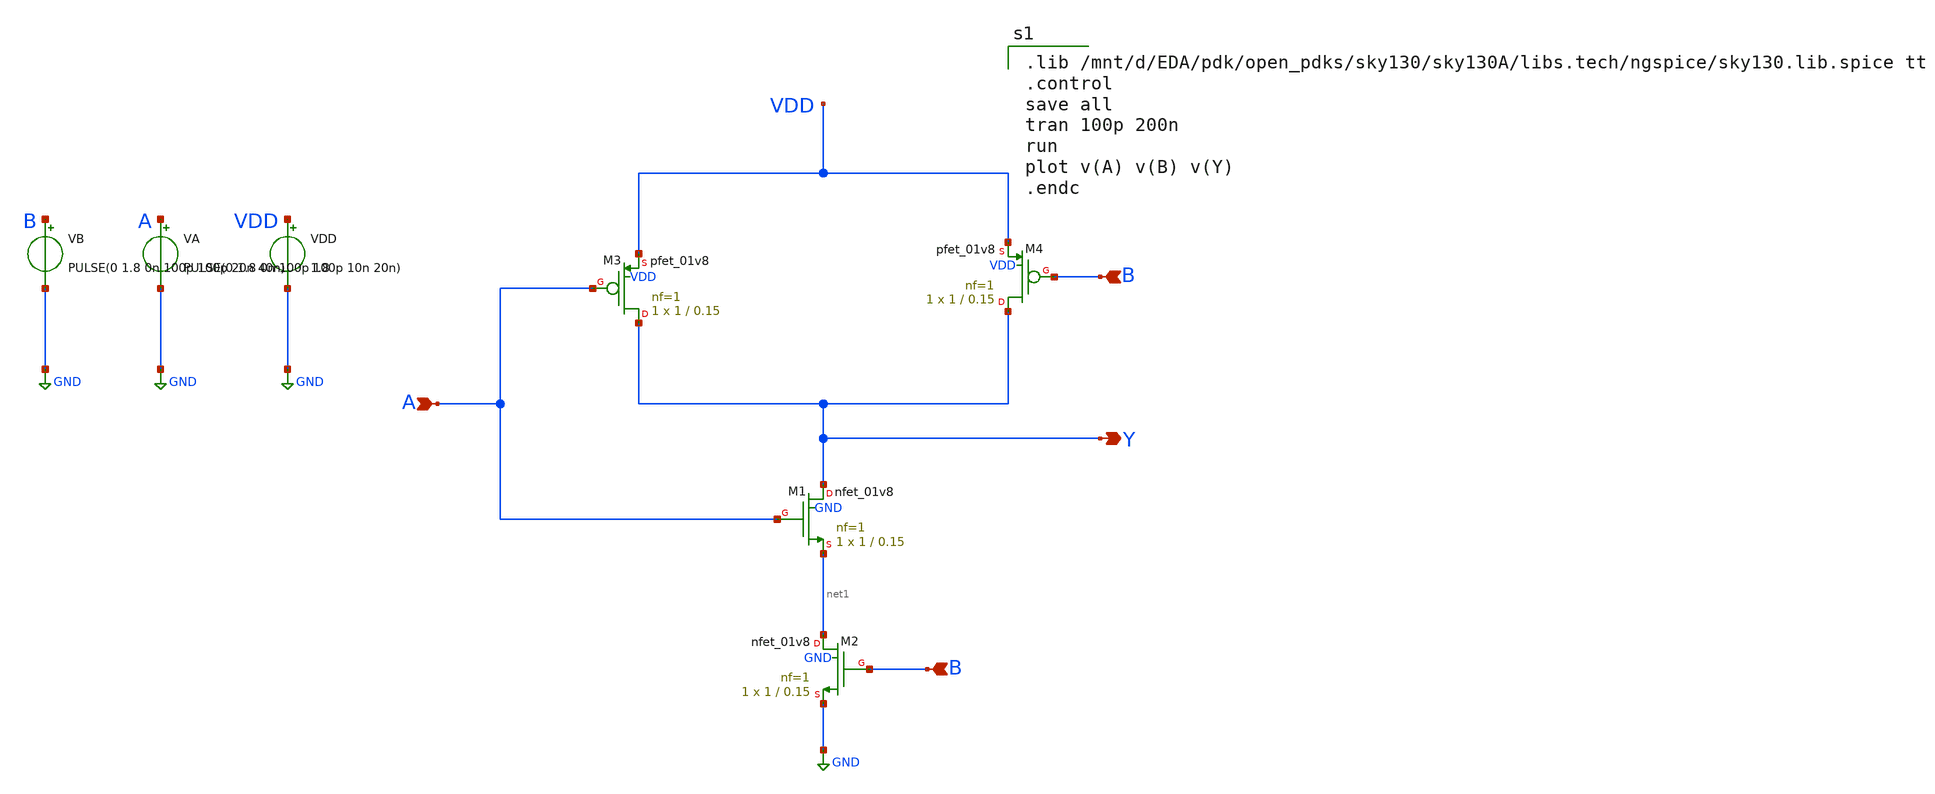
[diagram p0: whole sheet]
** sch_path: nand/nand.sch
**.subckt nand B A B Y
*.ipin B
*.ipin A
*.ipin B
*.opin Y
XM1 Y A net1 GND sky130_fd_pr__nfet_01v8 L=0.15 W=1 nf=1 ad='int((1 + 1)/2) * 1 / 1 * 0.29' as='int((1 + 2)/2) * 1 / 1 * 0.29'
+ pd='2*int((1 + 1)/2) * (1 / 1 + 0.29)' ps='2*int((1 + 2)/2) * (1 / 1 + 0.29)' nrd='0.29 / 1 ' nrs='0.29 / 1 '
+ sa=0 sb=0 sd=0 mult=1 m=1
XM2 net1 B GND GND sky130_fd_pr__nfet_01v8 L=0.15 W=1 nf=1 ad='int((1 + 1)/2) * 1 / 1 * 0.29' as='int((1 + 2)/2) * 1 / 1 * 0.29'
+ pd='2*int((1 + 1)/2) * (1 / 1 + 0.29)' ps='2*int((1 + 2)/2) * (1 / 1 + 0.29)' nrd='0.29 / 1 ' nrs='0.29 / 1 '
+ sa=0 sb=0 sd=0 mult=1 m=1
XM3 Y A VDD VDD sky130_fd_pr__pfet_01v8 L=0.15 W=1 nf=1 ad='int((1 + 1)/2) * 1 / 1 * 0.29' as='int((1 + 2)/2) * 1 / 1 * 0.29'
+ pd='2*int((1 + 1)/2) * (1 / 1 + 0.29)' ps='2*int((1 + 2)/2) * (1 / 1 + 0.29)' nrd='0.29 / 1 ' nrs='0.29 / 1 '
+ sa=0 sb=0 sd=0 mult=1 m=1
XM4 Y B VDD VDD sky130_fd_pr__pfet_01v8 L=0.15 W=1 nf=1 ad='int((1 + 1)/2) * 1 / 1 * 0.29' as='int((1 + 2)/2) * 1 / 1 * 0.29'
+ pd='2*int((1 + 1)/2) * (1 / 1 + 0.29)' ps='2*int((1 + 2)/2) * (1 / 1 + 0.29)' nrd='0.29 / 1 ' nrs='0.29 / 1 '
+ sa=0 sb=0 sd=0 mult=1 m=1
VDD VDD GND 1.8
VA A GND PULSE(0 1.8 0n 100p 100p 10n 20n)
VB B GND PULSE(0 1.8 0n 100p 100p 20n 40n)
**** begin user architecture code

.lib /mnt/d/EDA/pdk/open_pdks/sky130/sky130A/libs.tech/ngspice/sky130.lib.spice tt
.control
save all
tran 100p 200n
run
plot v(A) v(B) v(Y)
.endc

**** end user architecture code
**.ends
.GLOBAL GND
.end
